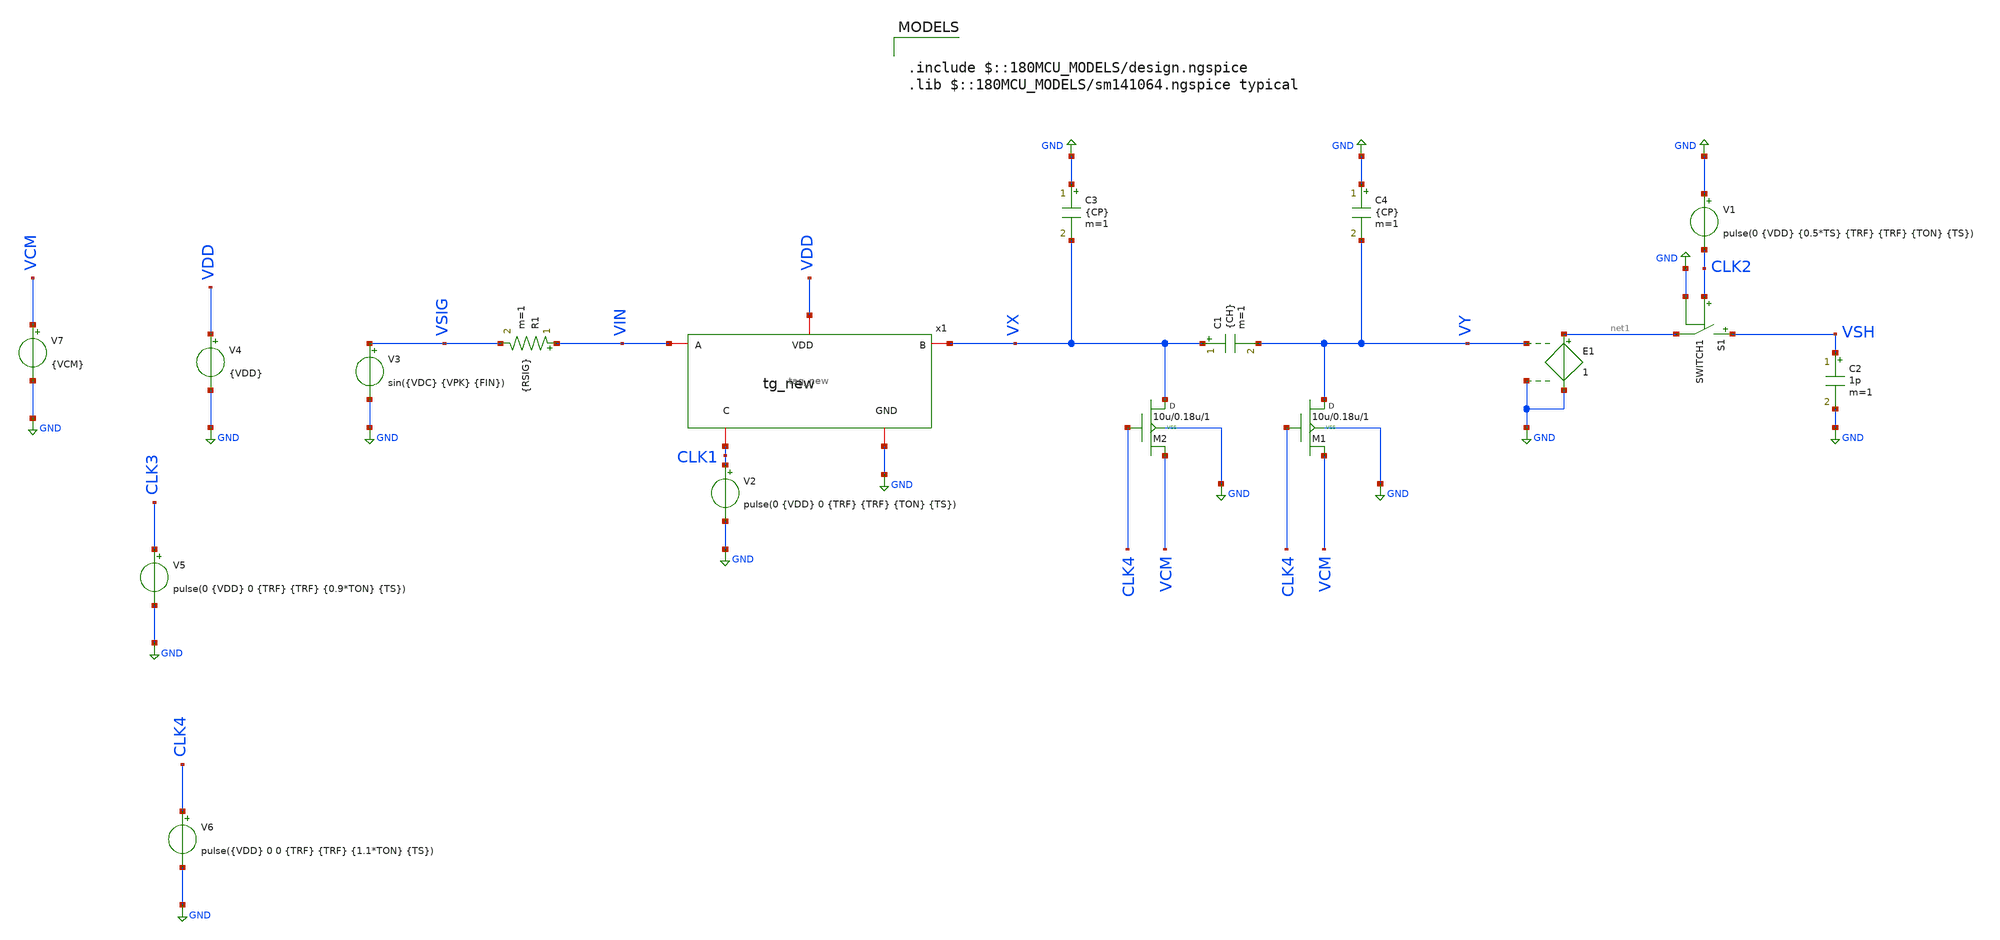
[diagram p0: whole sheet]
** sch_path: Designs/lab3_part2.sch
**.subckt lab3_part2
E1 net1 GND VY GND 1
S1 VSH net1 CLK2 GND SWITCH1
C2 VSH GND 1p m=1
V1 GND CLK2 pulse(0 {VDD} {0.5*TS} {TRF} {TRF} {TON} {TS})
V2 CLK1 GND pulse(0 {VDD} 0 {TRF} {TRF} {TON} {TS})
R1 VIN VSIG {RSIG} m=1
V3 VSIG GND sin({VDC} {VPK} {FIN})
V4 VDD GND {VDD}
x1 CLK1 GND VIN VX VDD tag_new W_N=10u L_N=0.18u W_P=10u L_P=0.18u
C3 GND VX {CP} m=1
M2 VX CLK4 VCM VSS nmos w=10u l=0.18u m=1
C1 VX VY {CH} m=1
C4 GND VY {CP} m=1
M1 VY CLK4 VCM VSS nmos w=10u l=0.18u m=1
V5 CLK3 GND pulse(0 {VDD} 0 {TRF} {TRF} {0.9*TON} {TS})
V6 CLK4 GND pulse({VDD} 0 0 {TRF} {TRF} {1.1*TON} {TS})
V7 VCM GND {VCM}
**** begin user architecture code




*These are the values of the parameters to be used
.param TS=1u
.param CH=1p CP={0.1*CH} RSIG=1k TON={0.4*TS} TRF=1n NCYC=5 NFFT=256 FIN={(NCYC/NFFT)/TS}
.param VDD=2 VDC={VDD/2} VCM={VDD/2} VPK={VDD/4} TDROP={0.5/FIN} TSTOP={(NCYC/FIN)+TDROP}
.param W_N=10u L_N=0.28u W_P=10u L_P=0.28u

*Analysis setup and control statements
.tran 25n {TSTOP} {TDROP}
.options filetype=ascii
*.options reltol=0.1u vntol=0.11u abstol=1p

*Required model for the switch
.model SWITCH1 sw vt={VDD/2}

.model nmos nmos

*save all voltages and currents
.save all




.include $::180MCU_MODELS/design.ngspice
.lib $::180MCU_MODELS/sm141064.ngspice typical

**** end user architecture code
**.ends

* expanding   symbol:  /home/tare/Desktop/Analog design/tag_new.sym # of pins=5
** sym_path: Designs/tag_new.sym
** sch_path: Designs/tag_new.sch
.subckt tag_new C GND A B VDD  W_N=10u L_N=0.18u W_P=10u L_P=0.18u
*.iopin B
*.iopin GND
*.iopin A
*.iopin VDD
*.iopin C
E1 net1 VDD C GND -1
XM3 B C A GND nmos_3p3_sab L=0.28u W=10u nf=1 ad='int((nf+1)/2) * W/nf * 0.18u' as='int((nf+2)/2) * W/nf * 0.18u'
+ pd='2*int((nf+1)/2) * (W/nf + 0.18u)' ps='2*int((nf+2)/2) * (W/nf + 0.18u)' nrd='0.18u / W' nrs='0.18u / W'
+ sa=0 sb=0 sd=0 m=1
XM1 B net1 A VDD pmos_3p3_sab L=0.28u W=10u nf=1 ad='int((nf+1)/2) * W/nf * 0.18u' as='int((nf+2)/2) * W/nf * 0.18u'
+ pd='2*int((nf+1)/2) * (W/nf + 0.18u)' ps='2*int((nf+2)/2) * (W/nf + 0.18u)' nrd='0.18u / W' nrs='0.18u / W'
+ sa=0 sb=0 sd=0 m=1
.ends

.GLOBAL GND
.end
